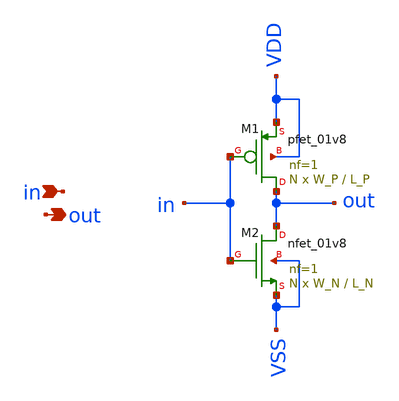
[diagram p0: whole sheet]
** sch_path: design/schematic/inv.sch
**.subckt inv in out
*.ipin in
*.opin out
XM2 out in VSS VSS sky130_fd_pr__nfet_01v8 L=L_N W=W_N nf=1 ad='int((nf+1)/2) * W/nf * 0.29' as='int((nf+2)/2) * W/nf * 0.29'
+ pd='2*int((nf+1)/2) * (W/nf + 0.29)' ps='2*int((nf+2)/2) * (W/nf + 0.29)' nrd='0.29 / W' nrs='0.29 / W'
+ sa=0 sb=0 sd=0 mult=N m=N
XM1 out in VDD VDD sky130_fd_pr__pfet_01v8 L=L_P W=W_P nf=1 ad='int((nf+1)/2) * W/nf * 0.29' as='int((nf+2)/2) * W/nf * 0.29'
+ pd='2*int((nf+1)/2) * (W/nf + 0.29)' ps='2*int((nf+2)/2) * (W/nf + 0.29)' nrd='0.29 / W' nrs='0.29 / W'
+ sa=0 sb=0 sd=0 mult=N m=N
**.ends
.end
